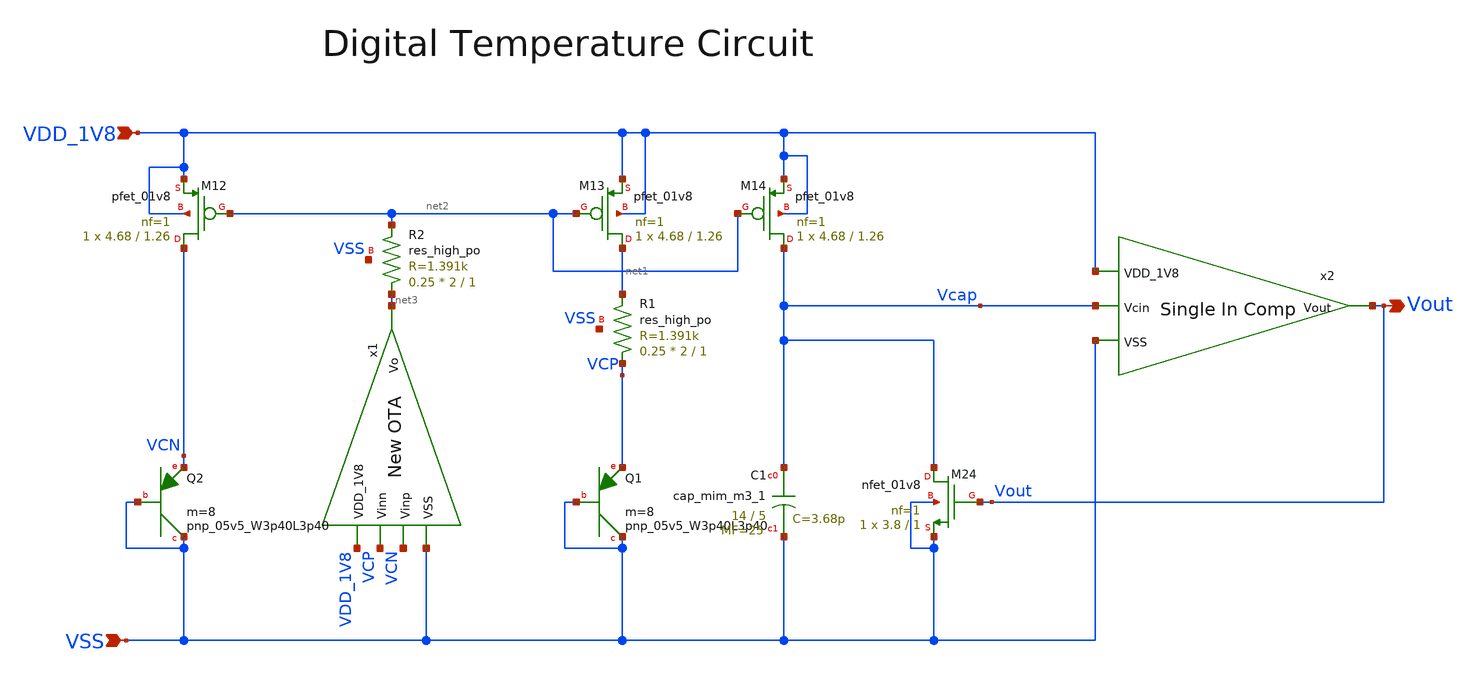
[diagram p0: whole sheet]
** sch_path: design/CNR_GR06_SKY130NM/CNR_GR06_main.sch
**.subckt CNR_GR06_main VDD_1V8 VSS Vout
*.ipin VDD_1V8
*.ipin VSS
*.opin Vout
XQ1 VSS VSS VCP sky130_fd_pr__pnp_05v5_W3p40L3p40 m=8
XR1 VCP net1 VSS sky130_fd_pr__res_high_po W=2 L=1 mult=0.25 m=0.25
XQ2 VSS VSS VCN sky130_fd_pr__pnp_05v5_W3p40L3p40 m=8
XM12 VCN net2 VDD_1V8 VDD_1V8 sky130_fd_pr__pfet_01v8 L=1.26 W=4.68 nf=1 ad='int((nf+1)/2) * W/nf * 0.29'
+ as='int((nf+2)/2) * W/nf * 0.29' pd='2*int((nf+1)/2) * (W/nf + 0.29)' ps='2*int((nf+2)/2) * (W/nf + 0.29)'
+ nrd='0.29 / W' nrs='0.29 / W' sa=0 sb=0 sd=0 mult=1 m=1
XM13 net1 net2 VDD_1V8 VDD_1V8 sky130_fd_pr__pfet_01v8 L=1.26 W=4.68 nf=1 ad='int((nf+1)/2) * W/nf * 0.29'
+ as='int((nf+2)/2) * W/nf * 0.29' pd='2*int((nf+1)/2) * (W/nf + 0.29)' ps='2*int((nf+2)/2) * (W/nf + 0.29)'
+ nrd='0.29 / W' nrs='0.29 / W' sa=0 sb=0 sd=0 mult=1 m=1
XM14 Vcap net2 VDD_1V8 VDD_1V8 sky130_fd_pr__pfet_01v8 L=1.26 W=4.68 nf=1 ad='int((nf+1)/2) * W/nf * 0.29'
+ as='int((nf+2)/2) * W/nf * 0.29' pd='2*int((nf+1)/2) * (W/nf + 0.29)' ps='2*int((nf+2)/2) * (W/nf + 0.29)'
+ nrd='0.29 / W' nrs='0.29 / W' sa=0 sb=0 sd=0 mult=1 m=1
XC1 Vcap VSS sky130_fd_pr__cap_mim_m3_1 W=14 L=5 MF=25 m=25
XM24 Vcap Vout VSS VSS sky130_fd_pr__nfet_01v8 L=1 W=3.8 nf=1 ad='int((nf+1)/2) * W/nf * 0.29' as='int((nf+2)/2) * W/nf * 0.29'
+ pd='2*int((nf+1)/2) * (W/nf + 0.29)' ps='2*int((nf+2)/2) * (W/nf + 0.29)' nrd='0.29 / W' nrs='0.29 / W'
+ sa=0 sb=0 sd=0 mult=1 m=1
XR2 net3 net2 VSS sky130_fd_pr__res_high_po W=2 L=1 mult=0.25 m=0.25
x1 VDD_1V8 VCP VCN net3 VSS New_OTA
x2 VDD_1V8 Vout Vcap VSS New_Comp
**.ends

* expanding   symbol:  CNR_GR06_SKY130NM/New_OTA.sym # of pins=5
** sym_path: design/CNR_GR06_SKY130NM/New_OTA.sym
** sch_path: design/CNR_GR06_SKY130NM/New_OTA.sch
.subckt New_OTA VDD_1V8 Vinn Vinp Vo VSS
*.ipin VDD_1V8
*.ipin VSS
*.ipin Vinn
*.ipin Vinp
*.opin Vo
XM16 net1 net1 VDD_1V8 VDD_1V8 sky130_fd_pr__pfet_01v8 L=1.26 W=7.68 nf=1 ad='int((nf+1)/2) * W/nf * 0.29'
+ as='int((nf+2)/2) * W/nf * 0.29' pd='2*int((nf+1)/2) * (W/nf + 0.29)' ps='2*int((nf+2)/2) * (W/nf + 0.29)'
+ nrd='0.29 / W' nrs='0.29 / W' sa=0 sb=0 sd=0 mult=1 m=1
XM17 net3 net1 VDD_1V8 VDD_1V8 sky130_fd_pr__pfet_01v8 L=1.26 W=7.68 nf=1 ad='int((nf+1)/2) * W/nf * 0.29'
+ as='int((nf+2)/2) * W/nf * 0.29' pd='2*int((nf+1)/2) * (W/nf + 0.29)' ps='2*int((nf+2)/2) * (W/nf + 0.29)'
+ nrd='0.29 / W' nrs='0.29 / W' sa=0 sb=0 sd=0 mult=1 m=1
XM18 net4 net2 net3 net3 sky130_fd_pr__pfet_01v8 L=1.26 W=7.68 nf=1 ad='int((nf+1)/2) * W/nf * 0.29'
+ as='int((nf+2)/2) * W/nf * 0.29' pd='2*int((nf+1)/2) * (W/nf + 0.29)' ps='2*int((nf+2)/2) * (W/nf + 0.29)'
+ nrd='0.29 / W' nrs='0.29 / W' sa=0 sb=0 sd=0 mult=1 m=1
XM19 net2 net2 net1 net1 sky130_fd_pr__pfet_01v8 L=1.26 W=7.68 nf=1 ad='int((nf+1)/2) * W/nf * 0.29'
+ as='int((nf+2)/2) * W/nf * 0.29' pd='2*int((nf+1)/2) * (W/nf + 0.29)' ps='2*int((nf+2)/2) * (W/nf + 0.29)'
+ nrd='0.29 / W' nrs='0.29 / W' sa=0 sb=0 sd=0 mult=1 m=1
XM20 Vo Vinp net4 net4 sky130_fd_pr__pfet_01v8 L=1.26 W=7.68 nf=1 ad='int((nf+1)/2) * W/nf * 0.29' as='int((nf+2)/2) * W/nf * 0.29'
+ pd='2*int((nf+1)/2) * (W/nf + 0.29)' ps='2*int((nf+2)/2) * (W/nf + 0.29)' nrd='0.29 / W' nrs='0.29 / W'
+ sa=0 sb=0 sd=0 mult=1 m=1
XM21 net5 Vinn net4 net4 sky130_fd_pr__pfet_01v8 L=1.26 W=7.68 nf=1 ad='int((nf+1)/2) * W/nf * 0.29'
+ as='int((nf+2)/2) * W/nf * 0.29' pd='2*int((nf+1)/2) * (W/nf + 0.29)' ps='2*int((nf+2)/2) * (W/nf + 0.29)'
+ nrd='0.29 / W' nrs='0.29 / W' sa=0 sb=0 sd=0 mult=1 m=1
XM22 Vo Vo VSS VSS sky130_fd_pr__nfet_01v8 L=2.7 W=2.84 nf=1 ad='int((nf+1)/2) * W/nf * 0.29' as='int((nf+2)/2) * W/nf * 0.29'
+ pd='2*int((nf+1)/2) * (W/nf + 0.29)' ps='2*int((nf+2)/2) * (W/nf + 0.29)' nrd='0.29 / W' nrs='0.29 / W'
+ sa=0 sb=0 sd=0 mult=1 m=1
XM23 net5 Vo VSS VSS sky130_fd_pr__nfet_01v8 L=2.7 W=2.84 nf=1 ad='int((nf+1)/2) * W/nf * 0.29' as='int((nf+2)/2) * W/nf * 0.29'
+ pd='2*int((nf+1)/2) * (W/nf + 0.29)' ps='2*int((nf+2)/2) * (W/nf + 0.29)' nrd='0.29 / W' nrs='0.29 / W'
+ sa=0 sb=0 sd=0 mult=1 m=1
XR3 VSS net2 VSS sky130_fd_pr__res_high_po W=2 L=0.5 mult=0.05 m=0.05
.ends


* expanding   symbol:  CNR_GR06_SKY130NM/New_Comp.sym # of pins=4
** sym_path: design/CNR_GR06_SKY130NM/New_Comp.sym
** sch_path: design/CNR_GR06_SKY130NM/New_Comp.sch
.subckt New_Comp VDD_1V8 Vout Vcin VSS
*.ipin VDD_1V8
*.ipin VSS
*.opin Vout
*.ipin Vcin
XM3 net1 net2 VDD_1V8 VDD_1V8 sky130_fd_pr__pfet_01v8 L=1 W=3.84 nf=1 ad='int((nf+1)/2) * W/nf * 0.29'
+ as='int((nf+2)/2) * W/nf * 0.29' pd='2*int((nf+1)/2) * (W/nf + 0.29)' ps='2*int((nf+2)/2) * (W/nf + 0.29)'
+ nrd='0.29 / W' nrs='0.29 / W' sa=0 sb=0 sd=0 mult=1 m=1
XM10 net3 Vcin VSS VSS sky130_fd_pr__nfet_01v8 L=1 W=1.6 nf=1 ad='int((nf+1)/2) * W/nf * 0.29' as='int((nf+2)/2) * W/nf * 0.29'
+ pd='2*int((nf+1)/2) * (W/nf + 0.29)' ps='2*int((nf+2)/2) * (W/nf + 0.29)' nrd='0.29 / W' nrs='0.29 / W'
+ sa=0 sb=0 sd=0 mult=1 m=1
XM11 Vcin Vcin VSS VSS sky130_fd_pr__nfet_01v8 L=1 W=1.6 nf=1 ad='int((nf+1)/2) * W/nf * 0.29' as='int((nf+2)/2) * W/nf * 0.29'
+ pd='2*int((nf+1)/2) * (W/nf + 0.29)' ps='2*int((nf+2)/2) * (W/nf + 0.29)' nrd='0.29 / W' nrs='0.29 / W'
+ sa=0 sb=0 sd=0 mult=1 m=1
XM5 net2 net2 VDD_1V8 net4 sky130_fd_pr__pfet_01v8 L=1 W=3.84 nf=1 ad='int((nf+1)/2) * W/nf * 0.29' as='int((nf+2)/2) * W/nf * 0.29'
+ pd='2*int((nf+1)/2) * (W/nf + 0.29)' ps='2*int((nf+2)/2) * (W/nf + 0.29)' nrd='0.29 / W' nrs='0.29 / W'
+ sa=0 sb=0 sd=0 mult=1 m=1
XM15 Vout net3 VDD_1V8 VDD_1V8 sky130_fd_pr__pfet_01v8 L=1 W=3.84 nf=1 ad='int((nf+1)/2) * W/nf * 0.29'
+ as='int((nf+2)/2) * W/nf * 0.29' pd='2*int((nf+1)/2) * (W/nf + 0.29)' ps='2*int((nf+2)/2) * (W/nf + 0.29)'
+ nrd='0.29 / W' nrs='0.29 / W' sa=0 sb=0 sd=0 mult=1 m=1
XM4 Vcin Vcin net1 net1 sky130_fd_pr__pfet_01v8 L=1 W=3.84 nf=1 ad='int((nf+1)/2) * W/nf * 0.29' as='int((nf+2)/2) * W/nf * 0.29'
+ pd='2*int((nf+1)/2) * (W/nf + 0.29)' ps='2*int((nf+2)/2) * (W/nf + 0.29)' nrd='0.29 / W' nrs='0.29 / W'
+ sa=0 sb=0 sd=0 mult=1 m=1
XM6 net3 Vcin net2 net2 sky130_fd_pr__pfet_01v8 L=1 W=3.84 nf=1 ad='int((nf+1)/2) * W/nf * 0.29' as='int((nf+2)/2) * W/nf * 0.29'
+ pd='2*int((nf+1)/2) * (W/nf + 0.29)' ps='2*int((nf+2)/2) * (W/nf + 0.29)' nrd='0.29 / W' nrs='0.29 / W'
+ sa=0 sb=0 sd=0 mult=1 m=1
XM8 Vout net3 VSS VSS sky130_fd_pr__nfet_01v8 L=1 W=1.6 nf=1 ad='int((nf+1)/2) * W/nf * 0.29' as='int((nf+2)/2) * W/nf * 0.29'
+ pd='2*int((nf+1)/2) * (W/nf + 0.29)' ps='2*int((nf+2)/2) * (W/nf + 0.29)' nrd='0.29 / W' nrs='0.29 / W'
+ sa=0 sb=0 sd=0 mult=1 m=1
.ends

.end
